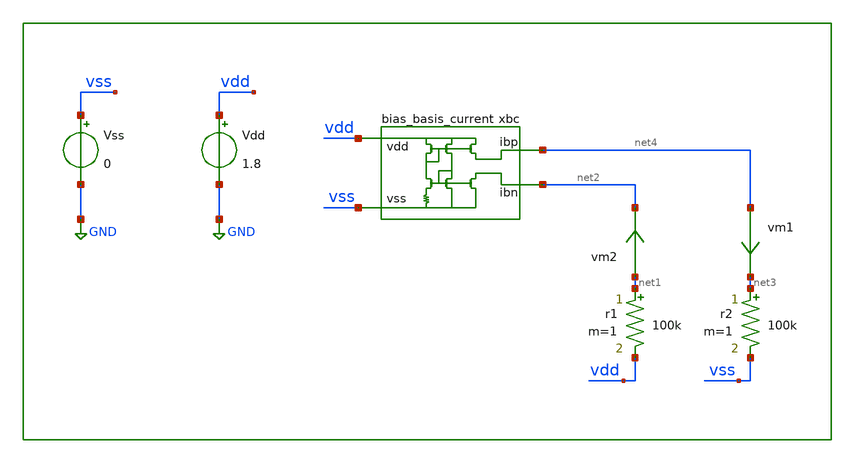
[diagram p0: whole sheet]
** sch_path: xschem/tb/bias/dc_bias_basis_current.sch
**.subckt dc_bias_basis_current
xbc vdd vss net4 net2 bias_basis_current
Vss vss GND 0
Vdd vdd GND 1.8
vm1 net4 net3 0
.save i(vm1)
r2 net3 vss 100k m=1
vm2 net1 net2 0
.save i(vm2)
r1 net1 vdd 100k m=1
**** begin user architecture code

.param MC_SWITCH=0
.options savecurrents

*.temp 27

.control
save all
op

let id_m4 = @m.xbc.xm4.msky130_fd_pr__pfet_01v8_lvt[id]
let id_m5 = @m.xbc.xm5.msky130_fd_pr__pfet_01v8_lvt[id]
let id_m7 = @m.xbc.xm7.msky130_fd_pr__nfet_01v8_lvt[id]
let ibp = vm1#branch
let ibn = vm2#branch

print id_m4
print id_m5
print id_m7

print ibp
print ibn
.endc



* FET CORNERS
*.include $::SKYWATER_MODELS/corners/tt.spice
*.include $::SKYWATER_MODELS/corners/ff.spice
.include $::SKYWATER_MODELS/corners/ss.spice
*.include $::SKYWATER_MODELS/corners/sf.spice
*.include $::SKYWATER_MODELS/corners/fs.spice

* TT + R + C
*.include $::SKYWATER_MODELS/corners/tt_rmax_cmax.spice
*.include $::SKYWATER_MODELS/corners/tt_rmin_cmin.spice
*.include $::SKYWATER_MODELS/corners/tt_rmax_cmin.spice
*.include $::SKYWATER_MODELS/corners/tt_rmin_cmax.spice

* FF + R + C
*.include $::SKYWATER_MODELS/corners/ff_rmax_cmax.spice
*.include $::SKYWATER_MODELS/corners/ff_rmin_cmin.spice
*.include $::SKYWATER_MODELS/corners/ff_rmax_cmin.spice
*.include $::SKYWATER_MODELS/corners/ff_rmin_cmax.spice


* SS + R + C
*.include $::SKYWATER_MODELS/corners/ss_rmax_cmax.spice
*.include $::SKYWATER_MODELS/corners/ss_rmin_cmin.spice
*.include $::SKYWATER_MODELS/corners/ss_rmax_cmin.spice
*.include $::SKYWATER_MODELS/corners/ss_rmin_cmax.spice

* SF + R + C
*.include $::SKYWATER_MODELS/corners/sf_rmax_cmax.spice
*.include $::SKYWATER_MODELS/corners/sf_rmin_cmin.spice
*.include $::SKYWATER_MODELS/corners/sf_rmax_cmin.spice
*.include $::SKYWATER_MODELS/corners/sf_rmin_cmax.spice

* FS + R + C
*.include $::SKYWATER_MODELS/corners/fs_rmax_cmax.spice
*.include $::SKYWATER_MODELS/corners/fs_rmin_cmin.spice
*.include $::SKYWATER_MODELS/corners/fs_rmax_cmin.spice
*.include $::SKYWATER_MODELS/corners/fs_rmin_cmax.spice

**** end user architecture code
**.ends

* expanding   symbol:  bias/bias_basis_current.sym # of pins=4
** sym_path: xschem/bias/bias_basis_current.sym
** sch_path: xschem/bias/bias_basis_current.sch
.subckt bias_basis_current vdd vss ibp ibn
*.iopin ibn
*.iopin vdd
*.iopin vss
*.iopin ibp
XM5 vbp vbp vdd vdd sky130_fd_pr__pfet_01v8_lvt L=1 W=1 nf=1 ad='int((nf+1)/2) * W/nf * 0.29' as='int((nf+2)/2) * W/nf * 0.29'
+ pd='2*int((nf+1)/2) * (W/nf + 0.29)' ps='2*int((nf+2)/2) * (W/nf + 0.29)' nrd='0.29 / W' nrs='0.29 / W'
+ sa=0 sb=0 sd=0 mult=8 m=8
XM4 vbn vbp vdd vdd sky130_fd_pr__pfet_01v8_lvt L=1 W=1 nf=1 ad='int((nf+1)/2) * W/nf * 0.29' as='int((nf+2)/2) * W/nf * 0.29'
+ pd='2*int((nf+1)/2) * (W/nf + 0.29)' ps='2*int((nf+2)/2) * (W/nf + 0.29)' nrd='0.29 / W' nrs='0.29 / W'
+ sa=0 sb=0 sd=0 mult=8 m=8
XM1 vbn vbn vss vss sky130_fd_pr__nfet_01v8_lvt L=0.5 W=1 nf=1 ad='int((nf+1)/2) * W/nf * 0.29' as='int((nf+2)/2) * W/nf * 0.29'
+ pd='2*int((nf+1)/2) * (W/nf + 0.29)' ps='2*int((nf+2)/2) * (W/nf + 0.29)' nrd='0.29 / W' nrs='0.29 / W'
+ sa=0 sb=0 sd=0 mult=8 m=8
XM2 vbp vbn vres vss sky130_fd_pr__nfet_01v8_lvt L=0.5 W=1 nf=1 ad='int((nf+1)/2) * W/nf * 0.29' as='int((nf+2)/2) * W/nf * 0.29'
+ pd='2*int((nf+1)/2) * (W/nf + 0.29)' ps='2*int((nf+2)/2) * (W/nf + 0.29)' nrd='0.29 / W' nrs='0.29 / W'
+ sa=0 sb=0 sd=0 mult=32 m=32
XM6 ibp vbp vdd vdd sky130_fd_pr__pfet_01v8_lvt L=1 W=1 nf=1 ad='int((nf+1)/2) * W/nf * 0.29' as='int((nf+2)/2) * W/nf * 0.29'
+ pd='2*int((nf+1)/2) * (W/nf + 0.29)' ps='2*int((nf+2)/2) * (W/nf + 0.29)' nrd='0.29 / W' nrs='0.29 / W'
+ sa=0 sb=0 sd=0 mult=2 m=2
XM3 ibn vbn vss vss sky130_fd_pr__nfet_01v8_lvt L=0.5 W=1 nf=1 ad='int((nf+1)/2) * W/nf * 0.29' as='int((nf+2)/2) * W/nf * 0.29'
+ pd='2*int((nf+1)/2) * (W/nf + 0.29)' ps='2*int((nf+2)/2) * (W/nf + 0.29)' nrd='0.29 / W' nrs='0.29 / W'
+ sa=0 sb=0 sd=0 mult=2 m=2
XM7 vsu vsu vss vss sky130_fd_pr__nfet_01v8_lvt L=0.3 W=1 nf=1 ad='int((nf+1)/2) * W/nf * 0.29' as='int((nf+2)/2) * W/nf * 0.29'
+ pd='2*int((nf+1)/2) * (W/nf + 0.29)' ps='2*int((nf+2)/2) * (W/nf + 0.29)' nrd='0.29 / W' nrs='0.29 / W'
+ sa=0 sb=0 sd=0 mult=1 m=1
XM8 vdd vsu vbn vss sky130_fd_pr__nfet_01v8_lvt L=0.3 W=1 nf=1 ad='int((nf+1)/2) * W/nf * 0.29' as='int((nf+2)/2) * W/nf * 0.29'
+ pd='2*int((nf+1)/2) * (W/nf + 0.29)' ps='2*int((nf+2)/2) * (W/nf + 0.29)' nrd='0.29 / W' nrs='0.29 / W'
+ sa=0 sb=0 sd=0 mult=1 m=1
XM9 vsu vsu net1 vdd sky130_fd_pr__pfet_01v8_lvt L=1 W=0.5 nf=1 ad='int((nf+1)/2) * W/nf * 0.29' as='int((nf+2)/2) * W/nf * 0.29'
+ pd='2*int((nf+1)/2) * (W/nf + 0.29)' ps='2*int((nf+2)/2) * (W/nf + 0.29)' nrd='0.29 / W' nrs='0.29 / W'
+ sa=0 sb=0 sd=0 mult=1 m=1
XM10 net1 net1 net2 vdd sky130_fd_pr__pfet_01v8_lvt L=1 W=0.5 nf=1 ad='int((nf+1)/2) * W/nf * 0.29' as='int((nf+2)/2) * W/nf * 0.29'
+ pd='2*int((nf+1)/2) * (W/nf + 0.29)' ps='2*int((nf+2)/2) * (W/nf + 0.29)' nrd='0.29 / W' nrs='0.29 / W'
+ sa=0 sb=0 sd=0 mult=1 m=1
XR2 vss vres vss sky130_fd_pr__res_xhigh_po W=0.35 L=14 mult=1 m=1
XR1 net2 vdd vss sky130_fd_pr__res_xhigh_po W=0.35 L=17 mult=1 m=1
.ends

.GLOBAL GND
.end
